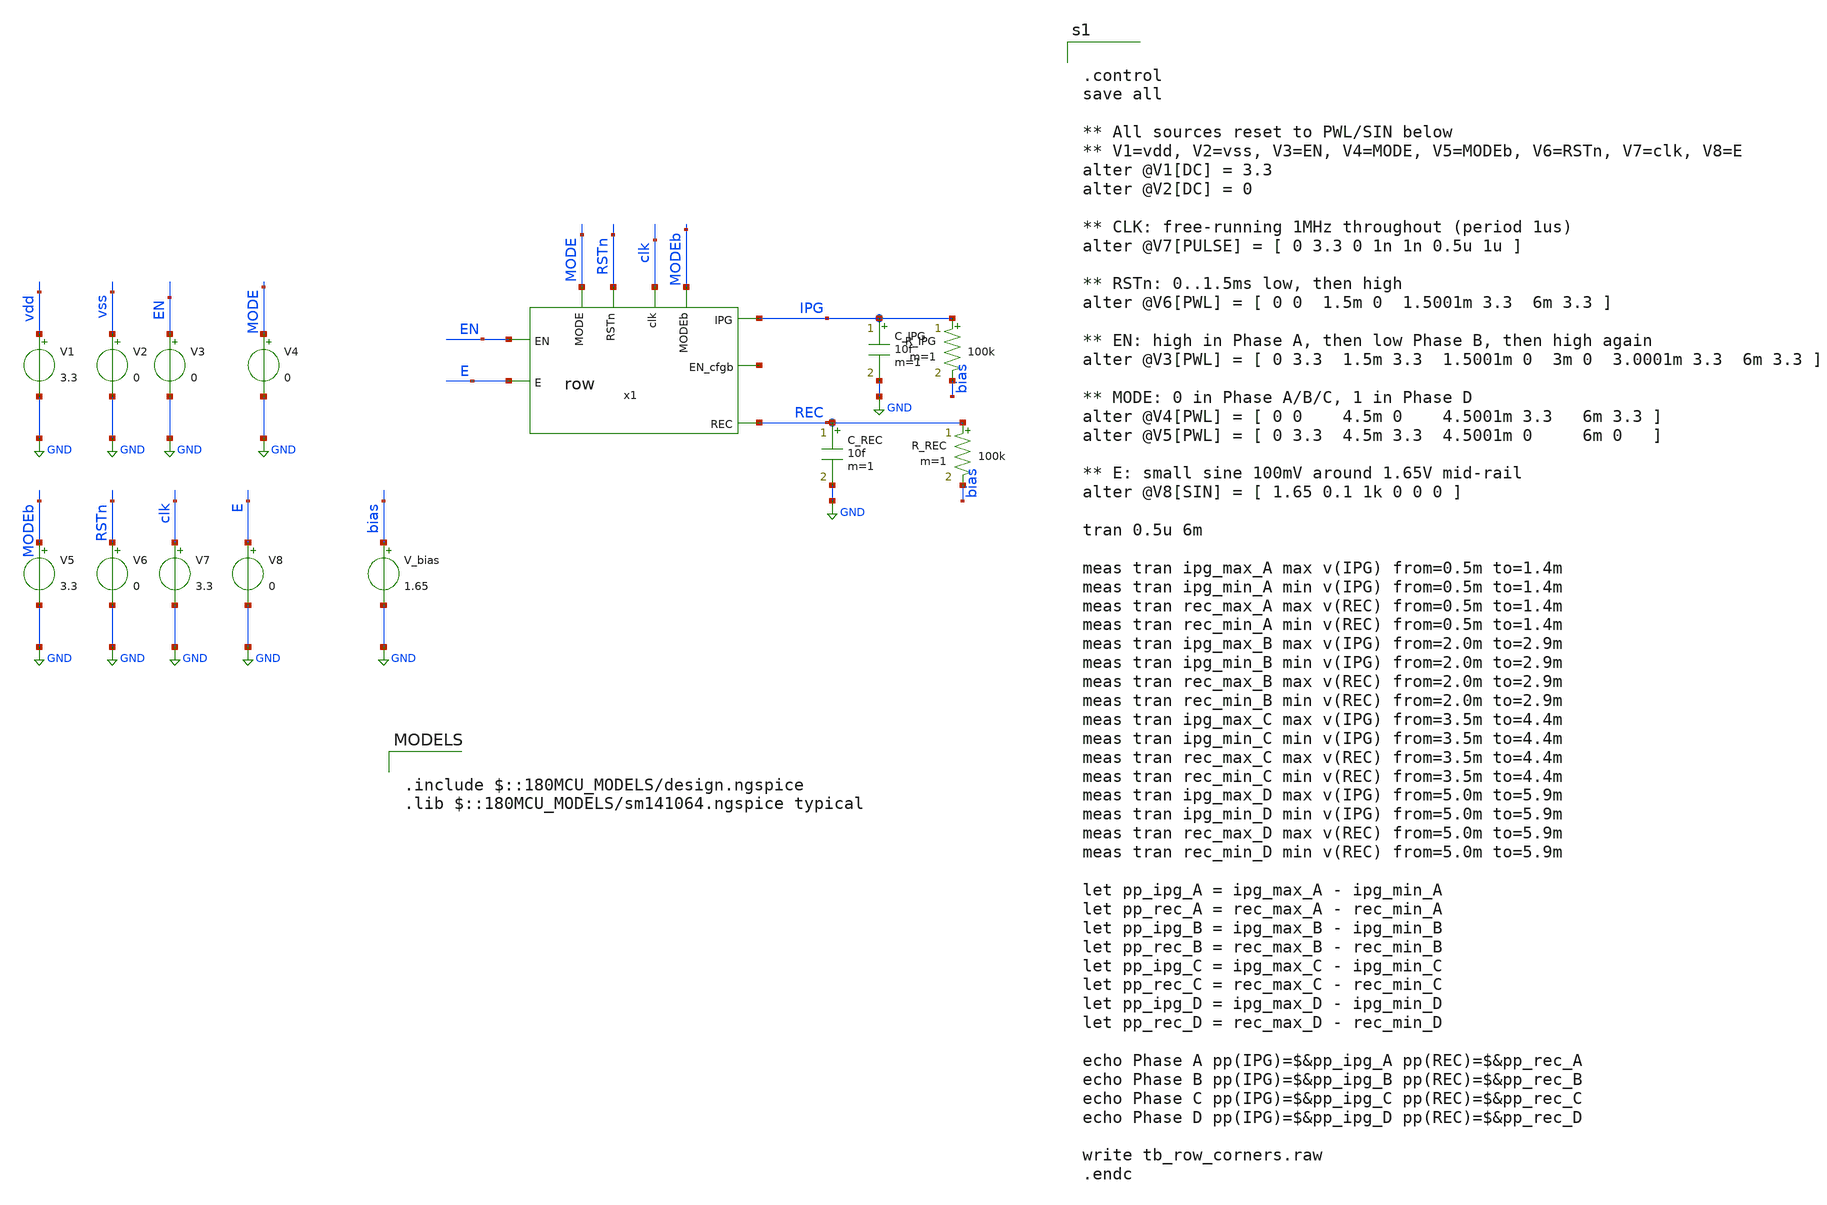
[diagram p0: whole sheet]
** sch_path: tb_row_corners.sch
**.subckt tb_row_corners
x1 IPG MODEb EN net1 clk E MODE RSTn REC row
V1 vdd GND 3.3
V2 vss GND 0
V3 EN GND 0
V4 MODE GND 0
V5 MODEb GND 3.3
V6 RSTn GND 0
V7 clk GND 3.3
V8 E GND 0
V_bias bias GND 1.65
C_REC REC GND 10f m=1
C_IPG IPG GND 10f m=1
R_IPG IPG bias 100k m=1
R_REC REC bias 100k m=1
**** begin user architecture code

.include $::180MCU_MODELS/design.ngspice
.lib $::180MCU_MODELS/sm141064.ngspice typical



.control
save all

** All sources reset to PWL/SIN below
** V1=vdd, V2=vss, V3=EN, V4=MODE, V5=MODEb, V6=RSTn, V7=clk, V8=E
alter @V1[DC] = 3.3
alter @V2[DC] = 0

** CLK: free-running 1MHz throughout (period 1us)
alter @V7[PULSE] = [ 0 3.3 0 1n 1n 0.5u 1u ]

** RSTn: 0..1.5ms low, then high
alter @V6[PWL] = [ 0 0  1.5m 0  1.5001m 3.3  6m 3.3 ]

** EN: high in Phase A, then low Phase B, then high again
alter @V3[PWL] = [ 0 3.3  1.5m 3.3  1.5001m 0  3m 0  3.0001m 3.3  6m 3.3 ]

** MODE: 0 in Phase A/B/C, 1 in Phase D
alter @V4[PWL] = [ 0 0    4.5m 0    4.5001m 3.3   6m 3.3 ]
alter @V5[PWL] = [ 0 3.3  4.5m 3.3  4.5001m 0     6m 0   ]

** E: small sine 100mV around 1.65V mid-rail
alter @V8[SIN] = [ 1.65 0.1 1k 0 0 0 ]

tran 0.5u 6m

meas tran ipg_max_A max v(IPG) from=0.5m to=1.4m
meas tran ipg_min_A min v(IPG) from=0.5m to=1.4m
meas tran rec_max_A max v(REC) from=0.5m to=1.4m
meas tran rec_min_A min v(REC) from=0.5m to=1.4m
meas tran ipg_max_B max v(IPG) from=2.0m to=2.9m
meas tran ipg_min_B min v(IPG) from=2.0m to=2.9m
meas tran rec_max_B max v(REC) from=2.0m to=2.9m
meas tran rec_min_B min v(REC) from=2.0m to=2.9m
meas tran ipg_max_C max v(IPG) from=3.5m to=4.4m
meas tran ipg_min_C min v(IPG) from=3.5m to=4.4m
meas tran rec_max_C max v(REC) from=3.5m to=4.4m
meas tran rec_min_C min v(REC) from=3.5m to=4.4m
meas tran ipg_max_D max v(IPG) from=5.0m to=5.9m
meas tran ipg_min_D min v(IPG) from=5.0m to=5.9m
meas tran rec_max_D max v(REC) from=5.0m to=5.9m
meas tran rec_min_D min v(REC) from=5.0m to=5.9m

let pp_ipg_A = ipg_max_A - ipg_min_A
let pp_rec_A = rec_max_A - rec_min_A
let pp_ipg_B = ipg_max_B - ipg_min_B
let pp_rec_B = rec_max_B - rec_min_B
let pp_ipg_C = ipg_max_C - ipg_min_C
let pp_rec_C = rec_max_C - rec_min_C
let pp_ipg_D = ipg_max_D - ipg_min_D
let pp_rec_D = rec_max_D - rec_min_D

echo Phase A pp(IPG)=$&pp_ipg_A pp(REC)=$&pp_rec_A
echo Phase B pp(IPG)=$&pp_ipg_B pp(REC)=$&pp_rec_B
echo Phase C pp(IPG)=$&pp_ipg_C pp(REC)=$&pp_rec_C
echo Phase D pp(IPG)=$&pp_ipg_D pp(REC)=$&pp_rec_D

write tb_row_corners.raw
.endc


**** end user architecture code
**.ends

* expanding   symbol:  row.sym # of pins=9
** sym_path: row.sym
** sch_path: row.sch
.subckt row IPG MODEb EN EN_cfgb clk E MODE RSTn REC
*.ipin EN
*.ipin clk
*.ipin MODEb
*.ipin MODE
*.ipin E
*.opin IPG
*.opin REC
*.ipin RSTn
*.opin EN_cfgb
x1 EN_cfg SW_IPG MODEb AND
x2 vdd RSTn EN EN_cfg EN_cfgb clk GND DFF
x3 IPG SW_IPG SW_IPGb E TGATE
x4 EN_cfg SW_REC MODE AND
x6 REC SW_REC SW_RECb E TGATE
x5 SW_IPGb SW_IPG INV
x7 SW_RECb SW_REC INV
.ends


* expanding   symbol:  AND/AND.sym # of pins=3
** sym_path: AND/AND.sym
** sch_path: AND/AND.sch
.subckt AND IN0 OUT IN1
*.opin OUT
*.ipin IN0
*.ipin IN1
XM1 net1 IN0 net2 GND nfet_03v3 L=0.28u W=1u nf=1 ad='int((nf+1)/2) * W/nf * 0.18u' as='int((nf+2)/2) * W/nf * 0.18u'
+ pd='2*int((nf+1)/2) * (W/nf + 0.18u)' ps='2*int((nf+2)/2) * (W/nf + 0.18u)' nrd='0.18u / W' nrs='0.18u / W'
+ sa=0 sb=0 sd=0 m=1
XM2 net2 IN1 GND GND nfet_03v3 L=0.28u W=1u nf=1 ad='int((nf+1)/2) * W/nf * 0.18u' as='int((nf+2)/2) * W/nf * 0.18u'
+ pd='2*int((nf+1)/2) * (W/nf + 0.18u)' ps='2*int((nf+2)/2) * (W/nf + 0.18u)' nrd='0.18u / W' nrs='0.18u / W'
+ sa=0 sb=0 sd=0 m=1
XM3 net1 IN0 vdd vdd pfet_03v3 L=0.28u W=1u nf=1 ad='int((nf+1)/2) * W/nf * 0.18u' as='int((nf+2)/2) * W/nf * 0.18u'
+ pd='2*int((nf+1)/2) * (W/nf + 0.18u)' ps='2*int((nf+2)/2) * (W/nf + 0.18u)' nrd='0.18u / W' nrs='0.18u / W'
+ sa=0 sb=0 sd=0 m=1
XM4 net1 IN1 vdd vdd pfet_03v3 L=0.28u W=1u nf=1 ad='int((nf+1)/2) * W/nf * 0.18u' as='int((nf+2)/2) * W/nf * 0.18u'
+ pd='2*int((nf+1)/2) * (W/nf + 0.18u)' ps='2*int((nf+2)/2) * (W/nf + 0.18u)' nrd='0.18u / W' nrs='0.18u / W'
+ sa=0 sb=0 sd=0 m=1
x1 OUT net1 INV
.ends


* expanding   symbol:  DFF/DFF.sym # of pins=7
** sym_path: DFF/DFF.sym
** sch_path: DFF/DFF.sch
.subckt DFF vdd RSTn D Q Qb CLK vss
*.ipin D
*.ipin CLK
*.ipin RSTn
*.opin Q
*.iopin vdd
*.iopin vss
*.opin Qb
XM1 net1 D net3 vss nfet_03v3 L=0.28u W=1u nf=1 ad='int((nf+1)/2) * W/nf * 0.18u' as='int((nf+2)/2) * W/nf * 0.18u'
+ pd='2*int((nf+1)/2) * (W/nf + 0.18u)' ps='2*int((nf+2)/2) * (W/nf + 0.18u)' nrd='0.18u / W' nrs='0.18u / W'
+ sa=0 sb=0 sd=0 m=1
XM2 net1 D net2 vdd pfet_03v3 L=0.28u W=1u nf=1 ad='int((nf+1)/2) * W/nf * 0.18u' as='int((nf+2)/2) * W/nf * 0.18u'
+ pd='2*int((nf+1)/2) * (W/nf + 0.18u)' ps='2*int((nf+2)/2) * (W/nf + 0.18u)' nrd='0.18u / W' nrs='0.18u / W'
+ sa=0 sb=0 sd=0 m=1
XM3 net2 c vdd vdd pfet_03v3 L=0.28u W=1u nf=1 ad='int((nf+1)/2) * W/nf * 0.18u' as='int((nf+2)/2) * W/nf * 0.18u'
+ pd='2*int((nf+1)/2) * (W/nf + 0.18u)' ps='2*int((nf+2)/2) * (W/nf + 0.18u)' nrd='0.18u / W' nrs='0.18u / W'
+ sa=0 sb=0 sd=0 m=1
XM4 net3 cbar vss vss nfet_03v3 L=0.28u W=1u nf=1 ad='int((nf+1)/2) * W/nf * 0.18u' as='int((nf+2)/2) * W/nf * 0.18u'
+ pd='2*int((nf+1)/2) * (W/nf + 0.18u)' ps='2*int((nf+2)/2) * (W/nf + 0.18u)' nrd='0.18u / W' nrs='0.18u / W'
+ sa=0 sb=0 sd=0 m=1
XM5 cbar CLK vss vss nfet_03v3 L=0.28u W=1u nf=1 ad='int((nf+1)/2) * W/nf * 0.18u' as='int((nf+2)/2) * W/nf * 0.18u'
+ pd='2*int((nf+1)/2) * (W/nf + 0.18u)' ps='2*int((nf+2)/2) * (W/nf + 0.18u)' nrd='0.18u / W' nrs='0.18u / W'
+ sa=0 sb=0 sd=0 m=1
XM6 cbar CLK vdd vdd pfet_03v3 L=0.28u W=1u nf=1 ad='int((nf+1)/2) * W/nf * 0.18u' as='int((nf+2)/2) * W/nf * 0.18u'
+ pd='2*int((nf+1)/2) * (W/nf + 0.18u)' ps='2*int((nf+2)/2) * (W/nf + 0.18u)' nrd='0.18u / W' nrs='0.18u / W'
+ sa=0 sb=0 sd=0 m=1
XM7 c cbar vss vss nfet_03v3 L=0.28u W=1u nf=1 ad='int((nf+1)/2) * W/nf * 0.18u' as='int((nf+2)/2) * W/nf * 0.18u'
+ pd='2*int((nf+1)/2) * (W/nf + 0.18u)' ps='2*int((nf+2)/2) * (W/nf + 0.18u)' nrd='0.18u / W' nrs='0.18u / W'
+ sa=0 sb=0 sd=0 m=1
XM8 c cbar vdd vdd pfet_03v3 L=0.28u W=1u nf=1 ad='int((nf+1)/2) * W/nf * 0.18u' as='int((nf+2)/2) * W/nf * 0.18u'
+ pd='2*int((nf+1)/2) * (W/nf + 0.18u)' ps='2*int((nf+2)/2) * (W/nf + 0.18u)' nrd='0.18u / W' nrs='0.18u / W'
+ sa=0 sb=0 sd=0 m=1
XM11 net5 RSTn net4 vss nfet_03v3 L=0.28u W=1u nf=1 ad='int((nf+1)/2) * W/nf * 0.18u' as='int((nf+2)/2) * W/nf * 0.18u'
+ pd='2*int((nf+1)/2) * (W/nf + 0.18u)' ps='2*int((nf+2)/2) * (W/nf + 0.18u)' nrd='0.18u / W' nrs='0.18u / W'
+ sa=0 sb=0 sd=0 m=1
XM12 net4 net6 vss vss nfet_03v3 L=0.28u W=1u nf=1 ad='int((nf+1)/2) * W/nf * 0.18u' as='int((nf+2)/2) * W/nf * 0.18u'
+ pd='2*int((nf+1)/2) * (W/nf + 0.18u)' ps='2*int((nf+2)/2) * (W/nf + 0.18u)' nrd='0.18u / W' nrs='0.18u / W'
+ sa=0 sb=0 sd=0 m=1
XM13 net5 RSTn vdd vdd pfet_03v3 L=0.28u W=1u nf=1 ad='int((nf+1)/2) * W/nf * 0.18u' as='int((nf+2)/2) * W/nf * 0.18u'
+ pd='2*int((nf+1)/2) * (W/nf + 0.18u)' ps='2*int((nf+2)/2) * (W/nf + 0.18u)' nrd='0.18u / W' nrs='0.18u / W'
+ sa=0 sb=0 sd=0 m=1
XM14 net5 net6 vdd vdd pfet_03v3 L=0.28u W=1u nf=1 ad='int((nf+1)/2) * W/nf * 0.18u' as='int((nf+2)/2) * W/nf * 0.18u'
+ pd='2*int((nf+1)/2) * (W/nf + 0.18u)' ps='2*int((nf+2)/2) * (W/nf + 0.18u)' nrd='0.18u / W' nrs='0.18u / W'
+ sa=0 sb=0 sd=0 m=1
XM15 net6 net1 vss vss nfet_03v3 L=0.28u W=1u nf=1 ad='int((nf+1)/2) * W/nf * 0.18u' as='int((nf+2)/2) * W/nf * 0.18u'
+ pd='2*int((nf+1)/2) * (W/nf + 0.18u)' ps='2*int((nf+2)/2) * (W/nf + 0.18u)' nrd='0.18u / W' nrs='0.18u / W'
+ sa=0 sb=0 sd=0 m=1
XM16 net6 net1 vdd vdd pfet_03v3 L=0.28u W=1u nf=1 ad='int((nf+1)/2) * W/nf * 0.18u' as='int((nf+2)/2) * W/nf * 0.18u'
+ pd='2*int((nf+1)/2) * (W/nf + 0.18u)' ps='2*int((nf+2)/2) * (W/nf + 0.18u)' nrd='0.18u / W' nrs='0.18u / W'
+ sa=0 sb=0 sd=0 m=1
XM21 net9 net7 net8 vss nfet_03v3 L=0.28u W=1u nf=1 ad='int((nf+1)/2) * W/nf * 0.18u' as='int((nf+2)/2) * W/nf * 0.18u'
+ pd='2*int((nf+1)/2) * (W/nf + 0.18u)' ps='2*int((nf+2)/2) * (W/nf + 0.18u)' nrd='0.18u / W' nrs='0.18u / W'
+ sa=0 sb=0 sd=0 m=1
XM22 net8 RSTn vss vss nfet_03v3 L=0.28u W=1u nf=1 ad='int((nf+1)/2) * W/nf * 0.18u' as='int((nf+2)/2) * W/nf * 0.18u'
+ pd='2*int((nf+1)/2) * (W/nf + 0.18u)' ps='2*int((nf+2)/2) * (W/nf + 0.18u)' nrd='0.18u / W' nrs='0.18u / W'
+ sa=0 sb=0 sd=0 m=1
XM23 net9 net7 vdd vdd pfet_03v3 L=0.28u W=1u nf=1 ad='int((nf+1)/2) * W/nf * 0.18u' as='int((nf+2)/2) * W/nf * 0.18u'
+ pd='2*int((nf+1)/2) * (W/nf + 0.18u)' ps='2*int((nf+2)/2) * (W/nf + 0.18u)' nrd='0.18u / W' nrs='0.18u / W'
+ sa=0 sb=0 sd=0 m=1
XM24 net9 RSTn vdd vdd pfet_03v3 L=0.28u W=1u nf=1 ad='int((nf+1)/2) * W/nf * 0.18u' as='int((nf+2)/2) * W/nf * 0.18u'
+ pd='2*int((nf+1)/2) * (W/nf + 0.18u)' ps='2*int((nf+2)/2) * (W/nf + 0.18u)' nrd='0.18u / W' nrs='0.18u / W'
+ sa=0 sb=0 sd=0 m=1
XM25 Q net9 vss vss nfet_03v3 L=0.28u W=1u nf=1 ad='int((nf+1)/2) * W/nf * 0.18u' as='int((nf+2)/2) * W/nf * 0.18u'
+ pd='2*int((nf+1)/2) * (W/nf + 0.18u)' ps='2*int((nf+2)/2) * (W/nf + 0.18u)' nrd='0.18u / W' nrs='0.18u / W'
+ sa=0 sb=0 sd=0 m=1
XM26 Q net9 vdd vdd pfet_03v3 L=0.28u W=1u nf=1 ad='int((nf+1)/2) * W/nf * 0.18u' as='int((nf+2)/2) * W/nf * 0.18u'
+ pd='2*int((nf+1)/2) * (W/nf + 0.18u)' ps='2*int((nf+2)/2) * (W/nf + 0.18u)' nrd='0.18u / W' nrs='0.18u / W'
+ sa=0 sb=0 sd=0 m=1
XM19 net7 net9 net11 vss nfet_03v3 L=0.28u W=1u nf=1 ad='int((nf+1)/2) * W/nf * 0.18u' as='int((nf+2)/2) * W/nf * 0.18u'
+ pd='2*int((nf+1)/2) * (W/nf + 0.18u)' ps='2*int((nf+2)/2) * (W/nf + 0.18u)' nrd='0.18u / W' nrs='0.18u / W'
+ sa=0 sb=0 sd=0 m=1
XM20 net7 net9 net10 vdd pfet_03v3 L=0.28u W=1u nf=1 ad='int((nf+1)/2) * W/nf * 0.18u' as='int((nf+2)/2) * W/nf * 0.18u'
+ pd='2*int((nf+1)/2) * (W/nf + 0.18u)' ps='2*int((nf+2)/2) * (W/nf + 0.18u)' nrd='0.18u / W' nrs='0.18u / W'
+ sa=0 sb=0 sd=0 m=1
XM31 net10 c vdd vdd pfet_03v3 L=0.28u W=1u nf=1 ad='int((nf+1)/2) * W/nf * 0.18u' as='int((nf+2)/2) * W/nf * 0.18u'
+ pd='2*int((nf+1)/2) * (W/nf + 0.18u)' ps='2*int((nf+2)/2) * (W/nf + 0.18u)' nrd='0.18u / W' nrs='0.18u / W'
+ sa=0 sb=0 sd=0 m=1
XM32 net11 cbar vss vss nfet_03v3 L=0.28u W=1u nf=1 ad='int((nf+1)/2) * W/nf * 0.18u' as='int((nf+2)/2) * W/nf * 0.18u'
+ pd='2*int((nf+1)/2) * (W/nf + 0.18u)' ps='2*int((nf+2)/2) * (W/nf + 0.18u)' nrd='0.18u / W' nrs='0.18u / W'
+ sa=0 sb=0 sd=0 m=1
XM35 net12 net9 vss vss nfet_03v3 L=0.28u W=1u nf=1 ad='int((nf+1)/2) * W/nf * 0.18u' as='int((nf+2)/2) * W/nf * 0.18u'
+ pd='2*int((nf+1)/2) * (W/nf + 0.18u)' ps='2*int((nf+2)/2) * (W/nf + 0.18u)' nrd='0.18u / W' nrs='0.18u / W'
+ sa=0 sb=0 sd=0 m=1
XM36 net12 net9 vdd vdd pfet_03v3 L=0.28u W=1u nf=1 ad='int((nf+1)/2) * W/nf * 0.18u' as='int((nf+2)/2) * W/nf * 0.18u'
+ pd='2*int((nf+1)/2) * (W/nf + 0.18u)' ps='2*int((nf+2)/2) * (W/nf + 0.18u)' nrd='0.18u / W' nrs='0.18u / W'
+ sa=0 sb=0 sd=0 m=1
XM37 Qb net12 vss vss nfet_03v3 L=0.28u W=1u nf=1 ad='int((nf+1)/2) * W/nf * 0.18u' as='int((nf+2)/2) * W/nf * 0.18u'
+ pd='2*int((nf+1)/2) * (W/nf + 0.18u)' ps='2*int((nf+2)/2) * (W/nf + 0.18u)' nrd='0.18u / W' nrs='0.18u / W'
+ sa=0 sb=0 sd=0 m=1
XM38 Qb net12 vdd vdd pfet_03v3 L=0.28u W=1u nf=1 ad='int((nf+1)/2) * W/nf * 0.18u' as='int((nf+2)/2) * W/nf * 0.18u'
+ pd='2*int((nf+1)/2) * (W/nf + 0.18u)' ps='2*int((nf+2)/2) * (W/nf + 0.18u)' nrd='0.18u / W' nrs='0.18u / W'
+ sa=0 sb=0 sd=0 m=1
XM9 net1 c net5 vss nfet_03v3 L=0.28u W=1u nf=1 ad='int((nf+1)/2) * W/nf * 0.18u' as='int((nf+2)/2) * W/nf * 0.18u'
+ pd='2*int((nf+1)/2) * (W/nf + 0.18u)' ps='2*int((nf+2)/2) * (W/nf + 0.18u)' nrd='0.18u / W' nrs='0.18u / W'
+ sa=0 sb=0 sd=0 m=1
XM10 net1 cbar net5 vdd pfet_03v3 L=0.28u W=1u nf=1 ad='int((nf+1)/2) * W/nf * 0.18u' as='int((nf+2)/2) * W/nf * 0.18u'
+ pd='2*int((nf+1)/2) * (W/nf + 0.18u)' ps='2*int((nf+2)/2) * (W/nf + 0.18u)' nrd='0.18u / W' nrs='0.18u / W'
+ sa=0 sb=0 sd=0 m=1
XM17 net6 c net7 vss nfet_03v3 L=0.28u W=1u nf=1 ad='int((nf+1)/2) * W/nf * 0.18u' as='int((nf+2)/2) * W/nf * 0.18u'
+ pd='2*int((nf+1)/2) * (W/nf + 0.18u)' ps='2*int((nf+2)/2) * (W/nf + 0.18u)' nrd='0.18u / W' nrs='0.18u / W'
+ sa=0 sb=0 sd=0 m=1
XM18 net6 cbar net7 vdd pfet_03v3 L=0.28u W=1u nf=1 ad='int((nf+1)/2) * W/nf * 0.18u' as='int((nf+2)/2) * W/nf * 0.18u'
+ pd='2*int((nf+1)/2) * (W/nf + 0.18u)' ps='2*int((nf+2)/2) * (W/nf + 0.18u)' nrd='0.18u / W' nrs='0.18u / W'
+ sa=0 sb=0 sd=0 m=1
.ends


* expanding   symbol:  TGATE/TGATE.sym # of pins=4
** sym_path: TGATE/TGATE.sym
** sch_path: TGATE/TGATE.sch
.subckt TGATE out c cbar in
*.ipin in
*.opin out
*.ipin cbar
*.ipin c
XM1 out cbar in VDD pfet_03v3 L=0.28u W=1u nf=1 ad='int((nf+1)/2) * W/nf * 0.18u' as='int((nf+2)/2) * W/nf * 0.18u'
+ pd='2*int((nf+1)/2) * (W/nf + 0.18u)' ps='2*int((nf+2)/2) * (W/nf + 0.18u)' nrd='0.18u / W' nrs='0.18u / W'
+ sa=0 sb=0 sd=0 m=1
XM2 out c in GND nfet_03v3 L=0.28u W=1u nf=1 ad='int((nf+1)/2) * W/nf * 0.18u' as='int((nf+2)/2) * W/nf * 0.18u'
+ pd='2*int((nf+1)/2) * (W/nf + 0.18u)' ps='2*int((nf+2)/2) * (W/nf + 0.18u)' nrd='0.18u / W' nrs='0.18u / W'
+ sa=0 sb=0 sd=0 m=1
.ends


* expanding   symbol:  AND/INV.sym # of pins=2
** sym_path: AND/INV.sym
** sch_path: AND/INV.sch
.subckt INV OUT IN
*.ipin IN
*.opin OUT
XM1 OUT IN VDD VDD pfet_03v3 L=0.28u W=1u nf=1 ad='int((nf+1)/2) * W/nf * 0.18u' as='int((nf+2)/2) * W/nf * 0.18u'
+ pd='2*int((nf+1)/2) * (W/nf + 0.18u)' ps='2*int((nf+2)/2) * (W/nf + 0.18u)' nrd='0.18u / W' nrs='0.18u / W'
+ sa=0 sb=0 sd=0 m=1
XM2 OUT IN GND GND nfet_03v3 L=0.28u W=0.5u nf=1 ad='int((nf+1)/2) * W/nf * 0.18u' as='int((nf+2)/2) * W/nf * 0.18u'
+ pd='2*int((nf+1)/2) * (W/nf + 0.18u)' ps='2*int((nf+2)/2) * (W/nf + 0.18u)' nrd='0.18u / W' nrs='0.18u / W'
+ sa=0 sb=0 sd=0 m=1
.ends

.GLOBAL GND
.GLOBAL vdd
.GLOBAL VDD
.end
